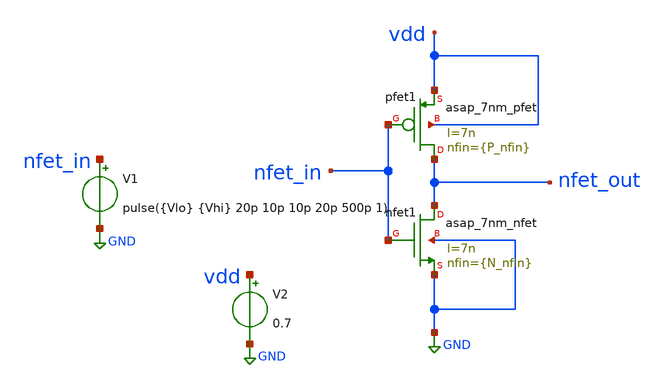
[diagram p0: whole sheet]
** sch_path: inverter_finfet.sch
* asap_7nm_nfet.sym:
* Copyright 2021 Stefan Frederik Schippers
* Licensed under the Apache License, Version 2.0 (the "License");
**.subckt inverter_finfet
Xpfet1 nfet_out nfet_in vdd vdd asap_7nm_pfet l=7n nfin={P_nfin}
Xnfet1 nfet_out nfet_in GND GND asap_7nm_nfet l=7n nfin={N_nfin}
V1 nfet_in GND pulse({Vlo} {Vhi} 20p 10p 10p 20p 500p 1)
V2 vdd GND 0.7
**** begin user architecture code



.param VDD = 0.7
* g3grau = 103+51+103+114+97+117=585  -> 58.5mV
.param Vuniq = 58.5m
.param Vlo = '0 + Vuniq'
.param Vhi = 'VDD + Vuniq'
.param N_nfin = 14
.param P_nfin = 14

.dc V1 0 0.7 1m
*.tran 0.1p 100p
.control
    *.dc V1 0 0.7 1m

    alterparam N_nfin=20
    alterparam P_nfin=20
    reset

    run
    meas dc v_th when nfet_out = nfet_in
    set xbrushwidth=3
    plot nfet_out nfet_in

    * generate gain curve
    let gain_av = abs(deriv(nfet_out))
    plot gain_av
    * get maximum gain
    meas dc max_gain max gain_av
    * get noise margins (input voltages outside transition region (gain<1))  ...!! NOT
+ max_gain*0.999
    let gain_target = 1.0
    meas dc vil find nfet_in when gain_av = gain_target cross=1
    meas dc voh find nfet_out when gain_av = gain_target cross=1
    meas dc vih find nfet_in when gain_av = gain_target cross=2
    meas dc vol find nfet_out when gain_av = gain_target cross=2
    let nmh = voh - vih
    let nml = vil - vol
    let nm = min(nmh,nml)
    print v_th max_gain vil voh vih vol nmh nml  nm
    * get gain>1 regions (for noise margin)

    * Transconductance  .. handle with care .. do these definitions make any sense?
    let id = -v2#branch
    let gm = real(deriv(id, nfet_in))
    meas dc gm_max max gm from = 1m to = 690m
    meas dc id_max max id
    plot gm
    let r_out = -deriv(nfet_out, id)
    plot r_out
    plot id

    * Transient measurements
    tran 1p 100p
    plot nfet_in nfet_out
    * Propagation delay (on VDD/2)
    meas tran tpir when nfet_in = 'VDD/2' rise = 1
    meas tran tpof when nfet_out = 'VDD/2' fall = 1
    let tplh = tpof - tpir
    meas tran tpor when nfet_in = 'VDD/2' fall = 1
    meas tran tpif when nfet_out = 'VDD/2' rise = 1
    let tphl = tpof - tpir
    let tp = (tplh + tphl) / 2
    print tplh tphl tp
    * Rise and fall times
    let thres = 0.1     ; 10%-90%
    let vl = VDD * thres
    let vh = VDD - vl
    meas tran tf1 when nfet_out = vh fall = 1
    meas tran tf2 when nfet_out = vl fall = 1
    meas tran tr1 when nfet_out = vl rise = 1
    meas tran tr2 when nfet_out = vh rise = 1
    let tf = tf2 - tf1
    let tr = tr2 - tr1
    let tdel = tr + tf
    let fmax = 1 / tdel
    print tr tf fmax

    let trans_current = -v2#branch
    meas tran id_charge integ trans_current from = 20p to = 60p
    let energy = id_charge * 0.7    ; VDD seems to be an array here??
    let power = energy
    * divide by 1s to normalize to 1Hz. Tutorial suggested 3/4 cycle which doesnt make sense (/ 40p)
    print energy power

.endc
.control
  pre_osdi $ASAP7_OSDI
.endc


**** end user architecture code
**.ends
.GLOBAL GND
**** begin user architecture code

.subckt asap_7nm_nfet S G D B l=@l nfin=@nfin
	nnmos_finfet S G D B BSIMCMG_osdi_N l=@l nfin=@nfin
.ends asap_7nm_nfet

.model BSIMCMG_osdi_N BSIMCMG_va (  TYPE = 1
************************************************************
*                         general                          *
************************************************************ version = 107             bulkmod = 1
*+               igcmod  = 1               igbmod  = 0              gidlmod = 1               iimod   = 0
*+               geomod  = 1               rdsmod  = 0              rgatemod= 0               rgeomod = 0
*+               shmod   = 0               nqsmod  = 0              coremod = 0               cgeomod = 0
*+               capmod  = 0               tnom    = 25             eot     = 1e-009          eotbox  = 1.4e-007
*+        eotacc  = 1e-010          tfin    = 6.5e-009       toxp    = 2.1e-009        nbody   = 1e+022
*+          phig    = 4.2466          epsrox  = 3.9            epsrsub = 11.9            easub   = 4.05
*+            ni0sub  = 1.1e+016        bg0sub  = 1.17           nc0sub  = 2.86e+025       nsd     = 2e+026
*+          ngate   = 0               nseg    = 5              l       = 2.1e-008        xl      = 1e-009
*+          lint    = -2e-009         dlc     = 0              dlbin   = 0               hfin    = 3.2e-008
*+        deltaw  = 0               deltawcv= 0              sdterm  = 0               epsrsp  = 3.9
*+             nfin    = 1 toxg    = 1.80e-009
************************************************************
*                            dc                            *
************************************************************ cit     = 0               cdsc    =
*+ 0.01            cdscd   = 0.01            dvt0    = 0.05           dvt1    = 0.47            phin    =
*+ 0.05            eta0    = 0.07            dsub    = 0.35           k1rsce  = 0               lpe0    = 0
*+               dvtshift= 0               qmfactor= 2.5            etaqm   = 0.54            qm0     = 0.001           pqm
*+     = 0.66            u0      = 0.0303         etamob  = 2               up      = 0               ua
*+      = 0.55            eu      = 1.2            ud      = 0               ucs     = 1
*+               rdswmin = 0               rdsw    = 200            wr      = 1               rswmin  = 0
*+               rdwmin  = 0               rshs    = 0              rshd    = 0               vsat    = 70000
*+           deltavsat= 0.2             ksativ  = 2              mexp    = 4               ptwg    = 30              pclm
*+    = 0.05            pclmg   = 0              pdibl1  = 0               pdibl2  = 0.002           drout
*+   = 1               pvag    = 0              fpitch  = 2.7e-008        rth0    = 0.225           cth0
*+    = 1.243e-006      wth0    = 2.6e-007       lcdscd  = 5e-005          lcdscdr = 5e-005          lrdsw
*+   = 0.2             lvsat   = 0
************************************************************
*                         leakage                          *
************************************************************ aigc    = 0.014           bigc    =
*+ 0.005           cigc    = 0.25            dlcigs  = 1e-009         dlcigd  = 1e-009          aigs    =
*+ 0.0115          aigd    = 0.0115          bigs    = 0.00332        bigd    = 0.00332         cigs    =
*+ 0.35            cigd    = 0.35            poxedge = 1.1            agidl   = 1e-012          agisl   =
*+ 1e-012          bgidl   = 10000000        bgisl   = 10000000       egidl   = 0.35            egisl   =
*+ 0.35
************************************************************
*                            rf                            *
************************************************************
************************************************************
*                         junction                         *
************************************************************
************************************************************
*                       capacitance                        *
************************************************************ cfs     = 0               cfd     = 0
*+               cgso    = 1.6e-010        cgdo    = 1.6e-010       cgsl    = 0               cgdl    = 0
*+               ckappas = 0.6             ckappad = 0.6            cgbo    = 0               cgbl    = 0
************************************************************
*                       temperature                        *
************************************************************ tbgasub = 0.000473        tbgbsub = 636
*+             kt1     = 0               kt1l    = 0              ute     = -0.7            utl     = 0
*+               ua1     = 0.001032        ud1     = 0              ucste   = -0.004775       at      = 0.001
*+           ptwgt   = 0.004           tmexp   = 0              prt     = 0               tgidl   = -0.007
*+          igt     = 2.5
************************************************************
*                          noise                           *
************************************************************
**)
.control
pre_osdi /home/vsduser/Documents/asap_7nm_Xschem/bsimcmg.osdi
.endc



.subckt asap_7nm_pfet S G D B l=@l nfin=@nfin
	npmos_finfet S G D B BSIMCMG_osdi_P l=@l nfin=@nfin
.ends asap_7nm_pfet

.model BSIMCMG_osdi_P BSIMCMG_va (  TYPE = 0

************************************************************
*                         general                          *
************************************************************ version = 107             bulkmod = 1
*+               igcmod  = 1               igbmod  = 0              gidlmod = 1               iimod   = 0
*+               geomod  = 1               rdsmod  = 0              rgatemod= 0               rgeomod = 0
*+               shmod   = 0               nqsmod  = 0              coremod = 0               cgeomod = 0
*+               capmod  = 0               tnom    = 25             eot     = 1e-009          eotbox  = 1.4e-007
*+        eotacc  = 3e-010          tfin    = 6.5e-009       toxp    = 2.1e-009        nbody   = 1e+022
*+          phig    = 4.9278          epsrox  = 3.9            epsrsub = 11.9            easub   = 4.05
*+            ni0sub  = 1.1e+016        bg0sub  = 1.17           nc0sub  = 2.86e+025       nsd     = 2e+026
*+          ngate   = 0               nseg    = 5              l       = 2.1e-008        xl      = 1e-009
*+          lint    = -2.5e-009       dlc     = 0              dlbin   = 0               hfin    = 3.2e-008
*+        deltaw  = 0               deltawcv= 0              sdterm  = 0               epsrsp  = 3.9
*+             nfin    = 1 toxg    = 1.8e-009
************************************************************
*                            dc                            *
************************************************************ cit     = 0               cdsc    =
*+ 0.003469        cdscd   = 0.001486        dvt0    = 0.05           dvt1    = 0.36            phin    = 0.05
*+            eta0    = 0.094           dsub    = 0.24           k1rsce  = 0               lpe0    = 0
*+               dvtshift= 0               qmfactor= 0              etaqm   = 0.54            qm0     = 2.183e-012      pqm
*+     = 0.66            u0      = 0.0237         etamob  = 4               up      = 0               ua
*+      = 1.133           eu      = 0.05           ud      = 0.0105          ucs     = 0.2672
*+          rdswmin = 0               rdsw    = 200            wr      = 1               rswmin  = 0
*+               rdwmin  = 0               rshs    = 0              rshd    = 0               vsat    = 60000
*+           deltavsat= 0.17            ksativ  = 1.592          mexp    = 2.491           ptwg    = 25              pclm
*+    = 0.01            pclmg   = 1              pdibl1  = 800             pdibl2  = 0.005704        drout
*+   = 4.97            pvag    = 200            fpitch  = 2.7e-008        rth0    = 0.15            cth0
*+    = 1.243e-006      wth0    = 2.6e-007       lcdscd  = 0               lcdscdr = 0               lrdsw
*+   = 1.3             lvsat   = 1441
************************************************************
*                         leakage                          *
************************************************************ aigc    = 0.007           bigc    =
*+ 0.0015          cigc    = 1               dlcigs  = 5e-009         dlcigd  = 5e-009          aigs    =
*+ 0.006           aigd    = 0.006           bigs    = 0.001944       bigd    = 0.001944        cigs    = 1
*+               cigd    = 1               poxedge = 1.152          agidl   = 2e-012          agisl   = 2e-012
*+          bgidl   = 1.5e+008        bgisl   = 1.5e+008       egidl   = 1.142           egisl   = 1.142
************************************************************
*                            rf                            *
************************************************************
************************************************************
*                         junction                         *
************************************************************
************************************************************
*                       capacitance                        *
************************************************************ cfs     = 0               cfd     = 0
*+               cgso    = 1.6e-010        cgdo    = 1.6e-010       cgsl    = 0               cgdl    = 0
*+               ckappas = 0.6             ckappad = 0.6            cgbo    = 0               cgbl    = 0
************************************************************
*                       temperature                        *
************************************************************ tbgasub = 0.000473        tbgbsub = 636
*+             kt1     = 0               kt1l    = 0              ute     = -1.2            utl     = 0
*+               ua1     = 0.001032        ud1     = 0              ucste   = -0.004775       at      = 0.001
*+           ptwgt   = 0.004           tmexp   = 0              prt     = 0               tgidl   = -0.007
*+          igt     = 2.5
************************************************************
*                          noise                           *
************************************************************
**)
.control
pre_osdi /home/vsduser/Documents/asap_7nm_Xschem/bsimcmg.osdi
.endc


**** end user architecture code
.end
